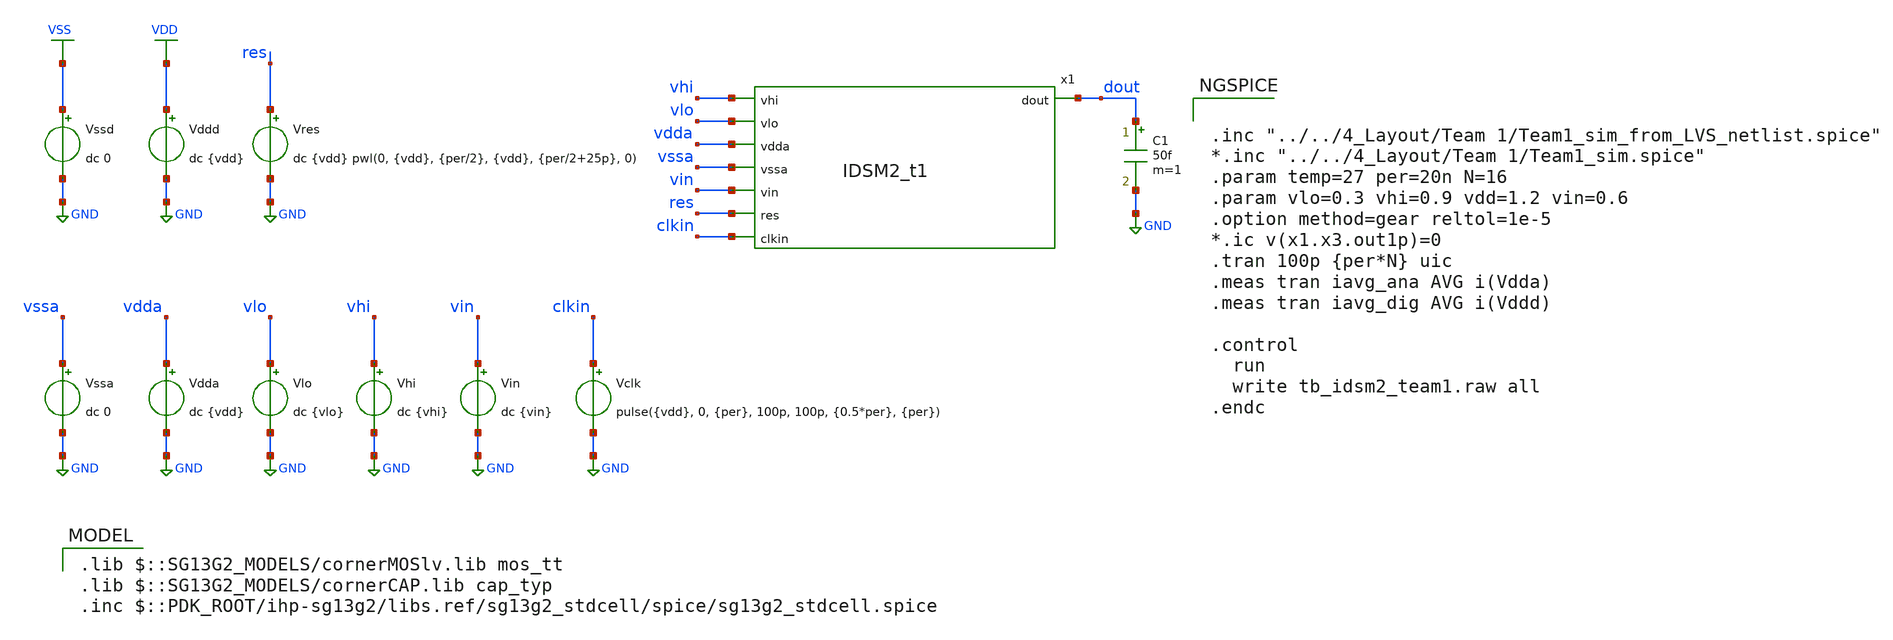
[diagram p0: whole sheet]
** sch_path: 5_Design/3_Real_circuits/tb_idsm2_team1.sch
**.subckt tb_idsm2_team1
Vin vin GND dc {vin}
Vssa vssa GND dc 0
Vres res GND dc {vdd} pwl(0, {vdd}, {per/2}, {vdd}, {per/2+25p}, 0)
Vclk clkin GND pulse({vdd}, 0, {per}, 100p, 100p, {0.5*per}, {per})
Vddd VDD GND dc {vdd}
Vssd VSS GND dc 0
Vdda vdda GND dc {vdd}
Vlo vlo GND dc {vlo}
Vhi vhi GND dc {vhi}
C1 dout GND 50f m=1
x1 vhi vlo vdda vssa vin dout res clkin IDSM2_t1
**** begin user architecture code


.inc "../../4_Layout/Team 1/Team1_sim_from_LVS_netlist.spice"
*.inc "../../4_Layout/Team 1/Team1_sim.spice"
.param temp=27 per=20n N=16
.param vlo=0.3 vhi=0.9 vdd=1.2 vin=0.6
.option method=gear reltol=1e-5
*.ic v(x1.x3.out1p)=0
.tran 100p {per*N} uic
.meas tran iavg_ana AVG i(Vdda)
.meas tran iavg_dig AVG i(Vddd)

.control
  run
  write tb_idsm2_team1.raw all
.endc


 .lib $::SG13G2_MODELS/cornerMOSlv.lib mos_tt
.lib $::SG13G2_MODELS/cornerCAP.lib cap_typ
.inc $::PDK_ROOT/ihp-sg13g2/libs.ref/sg13g2_stdcell/spice/sg13g2_stdcell.spice

**** end user architecture code
**.ends
.GLOBAL GND
.GLOBAL VDD
.GLOBAL VSS
.end
